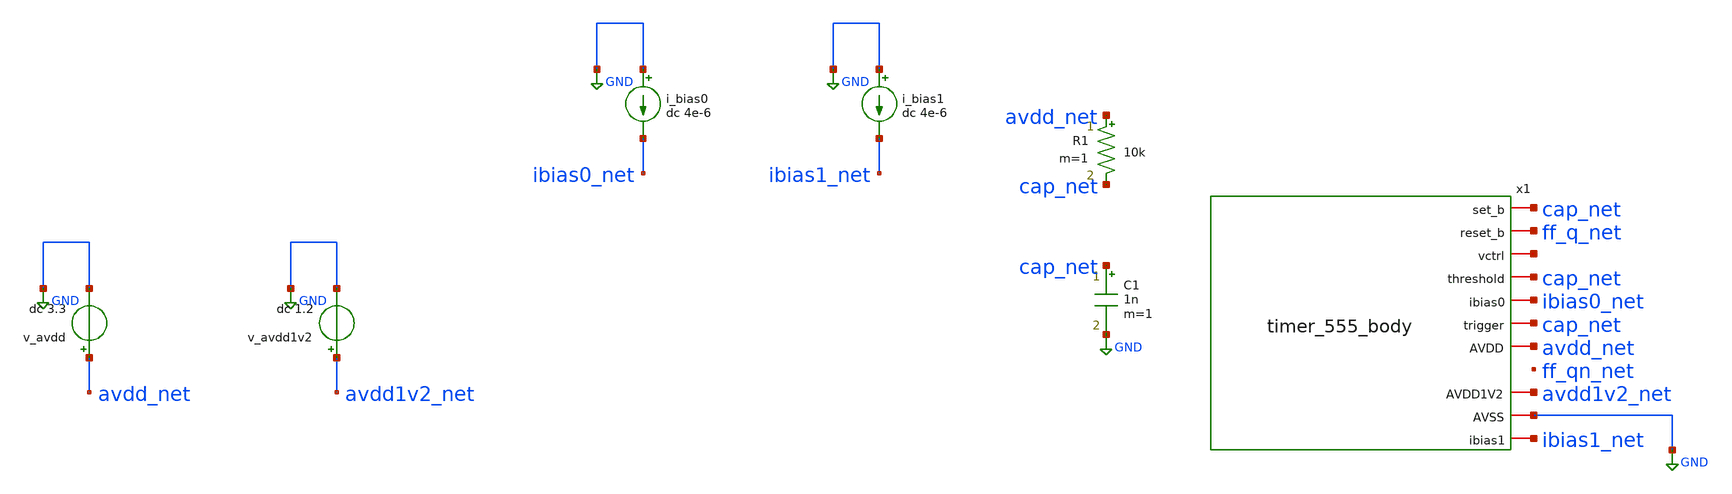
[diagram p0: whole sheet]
** sch_path: macros/timer_555_body/testbenches/xschem/tb_timer_555_body.sch
**.subckt tb_timer_555_body
v_avdd avdd_net GND dc 3.3
v_avdd1v2 avdd1v2_net GND dc 1.2
i_bias0 GND ibias0_net dc 4e-6
i_bias1 GND ibias1_net dc 4e-6
R1 avdd_net cap_net 10k m=1
C1 cap_net GND 1n m=1
x1 cap_net ff_q_net net1 cap_net ibias0_net cap_net avdd_net avdd1v2_net GND ibias1_net
+ timer_555_body
**** begin user architecture code


.lib $PDK_ROOT/$PDK/libs.tech/ngspice/models/cornerMOShv.lib mos_tt
.lib $PDK_ROOT/$PDK/libs.tech/ngspice/models/cornerMOSlv.lib mos_tt
.lib $PDK_ROOT/$PDK/libs.tech/ngspice/models/cornerRES.lib res_typ
.include $PDK_ROOT/$PDK/libs.ref/sg13cmos5l_stdcell/spice/sg13cmos5l_stdcell.spice




.op
.tran 10n 200u
.control
  run
  plot v(cap_net) v(ff_q_net) v(ff_qn_net)
.endc


**** end user architecture code
**.ends
.GLOBAL GND
.end
